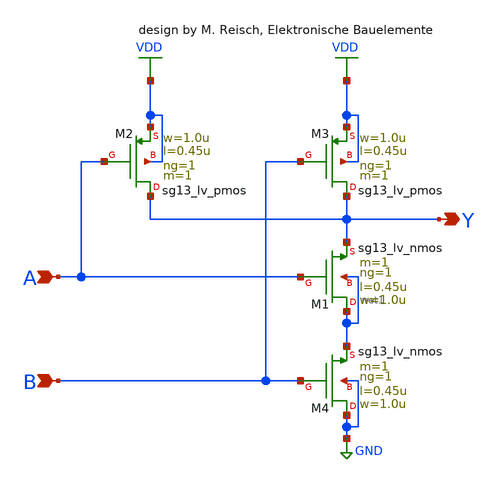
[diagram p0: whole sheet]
** sch_path: zip_meiners/ic_design/design_clkgen/nand/nand_gate.sch
**.subckt nand_gate A B Y
*.ipin A
*.ipin B
*.opin Y
XM1 net1 A Y net1 sg13_lv_nmos w=1.0u l=0.45u ng=1 m=1 mm_ok=1
XM2 Y A VDD VDD sg13_lv_pmos w=1.0u l=0.45u ng=1 m=1 mm_ok=1
XM3 Y B VDD VDD sg13_lv_pmos w=1.0u l=0.45u ng=1 m=1 mm_ok=1
XM4 GND B net1 GND sg13_lv_nmos w=1.0u l=0.45u ng=1 m=1 mm_ok=1
**.ends
.GLOBAL VDD
.GLOBAL GND
.end
